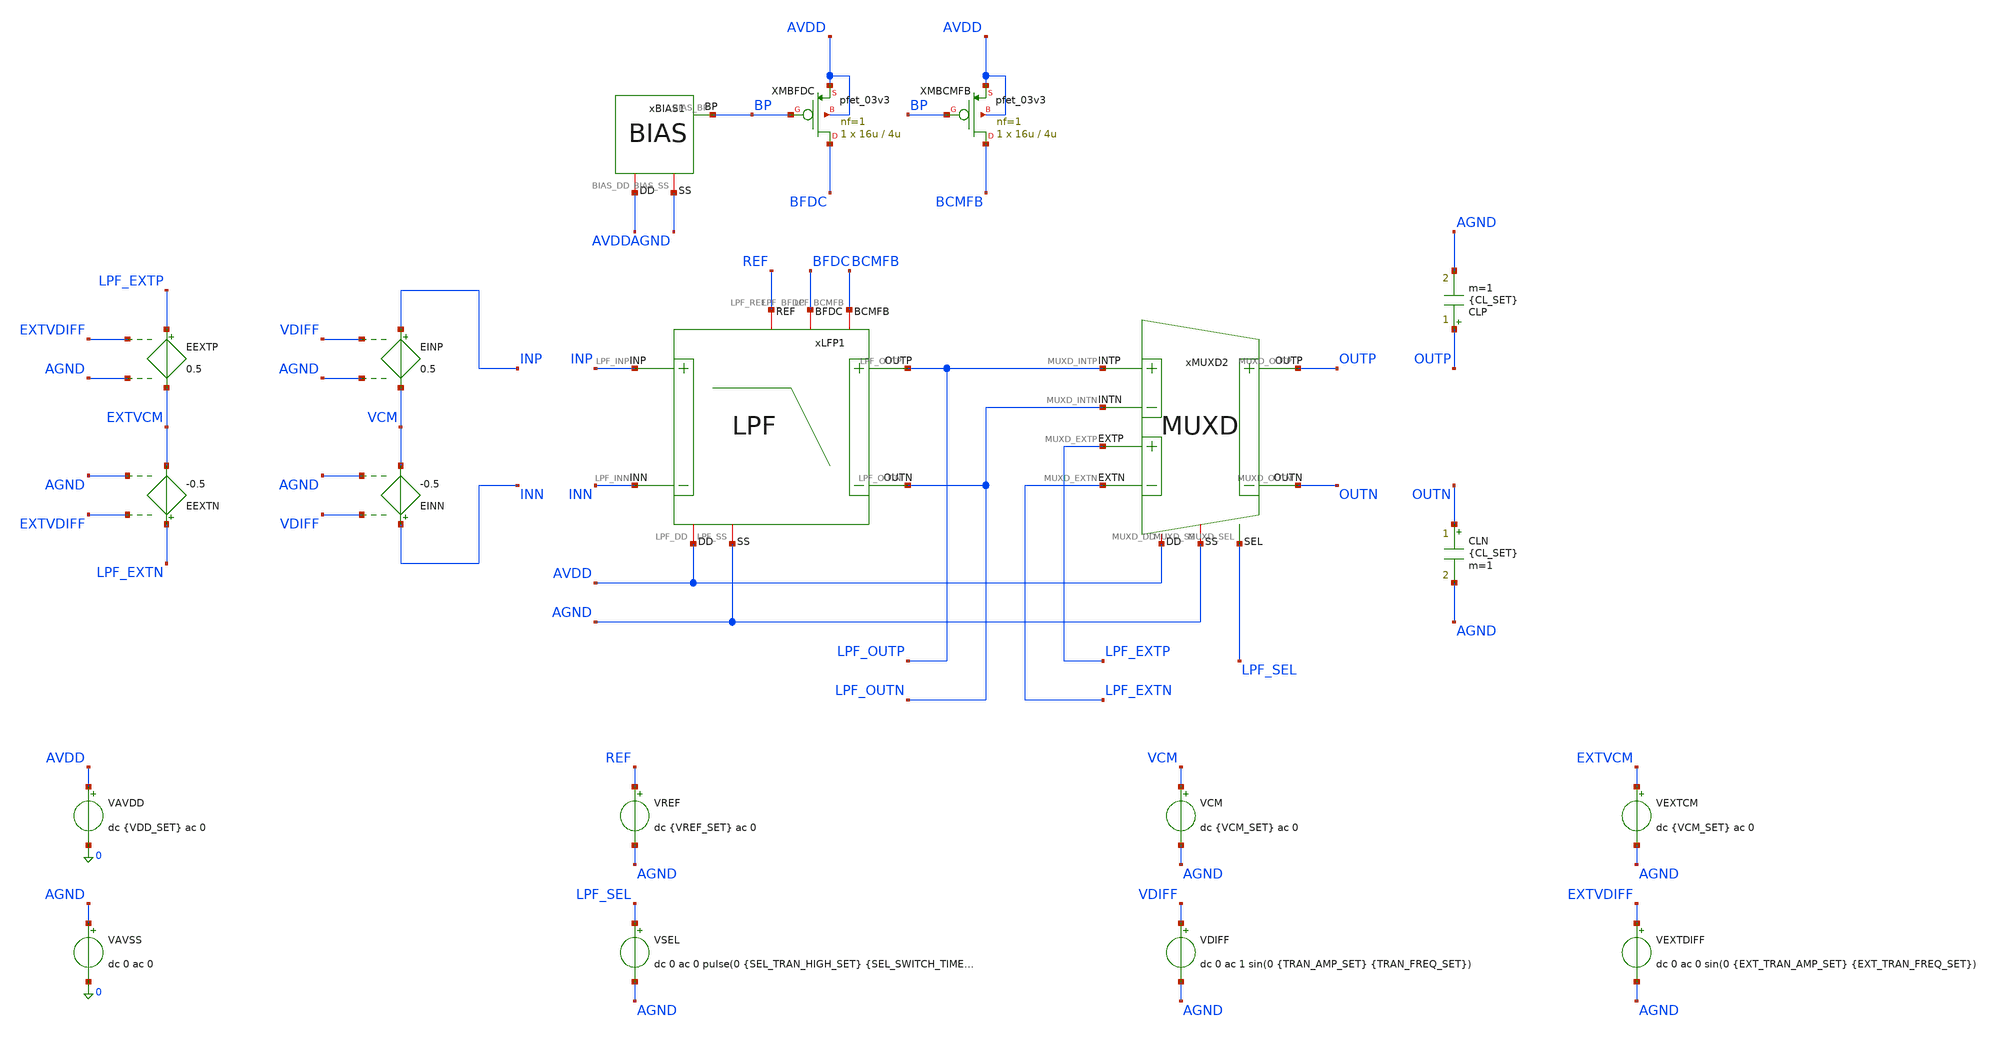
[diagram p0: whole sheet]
** sch_path: Design_Files/IC Design/Testbench/AFE_BLOCKS/LPF/LPF_TB_MC.sch
**.subckt LPF_TB_MC
CLP OUTP AGND {CL_SET} m=1
CLN OUTN AGND {CL_SET} m=1
xBIAS1 AVDD AGND BP BIAS
XMBFDC BFDC BP AVDD AVDD pfet_03v3 L=4u W=16u nf=1 ad='int((nf+1)/2) * W/nf * 0.18u' as='int((nf+2)/2) * W/nf * 0.18u'
+ pd='2*int((nf+1)/2) * (W/nf + 0.18u)' ps='2*int((nf+2)/2) * (W/nf + 0.18u)' nrd='0.18u / W' nrs='0.18u / W'
+ sa=0 sb=0 sd=0 m=1
XMBCMFB BCMFB BP AVDD AVDD pfet_03v3 L=4u W=16u nf=1 ad='int((nf+1)/2) * W/nf * 0.18u' as='int((nf+2)/2) * W/nf * 0.18u'
+ pd='2*int((nf+1)/2) * (W/nf + 0.18u)' ps='2*int((nf+2)/2) * (W/nf + 0.18u)' nrd='0.18u / W' nrs='0.18u / W'
+ sa=0 sb=0 sd=0 m=1
VAVDD AVDD 0 dc {VDD_SET} ac 0
.save i(vavdd)
VAVSS AGND 0 dc 0 ac 0
xLFP1 AVDD AGND INP INN LPF_OUTN BFDC LPF_OUTP BCMFB REF LPF
xMUXD2 AVDD AGND LPF_OUTP LPF_OUTN OUTN OUTP LPF_EXTP LPF_EXTN LPF_SEL MUXD
VCM VCM AGND dc {VCM_SET} ac 0
VDIFF VDIFF AGND dc 0 ac 1 sin(0 {TRAN_AMP_SET} {TRAN_FREQ_SET})
VREF REF AGND dc {VREF_SET} ac 0
VSEL LPF_SEL AGND dc 0 ac 0 pulse(0 {SEL_TRAN_HIGH_SET} {SEL_SWITCH_TIME_SET} 1u 1u 400m 800m)
VEXTCM EXTVCM AGND dc {VCM_SET} ac 0
VEXTDIFF EXTVDIFF AGND dc 0 ac 0 sin(0 {EXT_TRAN_AMP_SET} {EXT_TRAN_FREQ_SET})
EINP INP VCM VDIFF AGND 0.5
EINN INN VCM VDIFF AGND -0.5
EEXTP LPF_EXTP EXTVCM EXTVDIFF AGND 0.5
EEXTN LPF_EXTN EXTVCM EXTVDIFF AGND -0.5
**** begin user architecture code

* {MODELS_START}
.include $::180MCU_MODELS/design.ngspice

.param sw_stat_global=0
.param sw_stat_mismatch=1

.param mc_skew=3
.param res_mc_skew=3
.param cap_mc_skew=3

.lib $::180MCU_MODELS/sm141064.ngspice statistical
.lib $::180MCU_MODELS/sm141064.ngspice res_statistical
.lib $::180MCU_MODELS/sm141064.ngspice mimcap_statistical
.lib $::180MCU_MODELS/sm141064.ngspice cap_mim
.lib $::180MCU_MODELS/sm141064.ngspice bjt_statistical
* {MODELS_END}



* {SETUP_START}
.param VDD_SET=3.3
.param TEMP_SET=27

.param VCM_SET={VDD_SET/2}
.param VREF_SET={VDD_SET/2}

.param CL_SET=10p

.param LPF_GAIN_TARGET_SET=1
.param LPF_F1DB_TARGET_SET=150
.param LPF_F3DB_TARGET_SET=300

.param TRAN_AMP_SET=100m
.param TRAN_FREQ_SET=10

.param EXT_TRAN_AMP_SET=50m
.param EXT_TRAN_FREQ_SET=25

.param SEL_TRAN_HIGH_SET=0
.param SEL_SWITCH_TIME_SET=200m

.csparam MC_RUNS=200

.temp {TEMP_SET}

.options gmin=1e-12
.options rshunt=1e12
.options method=gear
* {SETUP_END}




* {MEAS_START}
.control

destroy all

set noaskquit
set wr_singlescale
unset wr_vecnames

option klu
option numdgt=15
option method=gear
option maxord=2
option plotwinsize=0

let mode_index=0

dowhile mode_index < 3

if mode_index = 0
set mode=mm
set tag=mm
alterparam sw_stat_global=0
alterparam sw_stat_mismatch=1
end

if mode_index = 1
set mode=gl
set tag=gl
alterparam sw_stat_global=1
alterparam sw_stat_mismatch=0
end

if mode_index = 2
set mode=full
set tag=full
alterparam sw_stat_global=1
alterparam sw_stat_mismatch=1
end

alterparam VDD_SET=3.3
alterparam TEMP_SET=27
alterparam SEL_TRAN_HIGH_SET=0
alterparam EXT_TRAN_AMP_SET=0

reset

shell mkdir -p /foss/designs/ECG_Acquisition_IC/Measurement_Results/IC_Simulation/AFE_BLOCKS/LPF/{$mode}.Result_txt
shell rm -f /foss/designs/ECG_Acquisition_IC/Measurement_Results/IC_Simulation/AFE_BLOCKS/LPF/{$mode}.Result_txt/{$tag}.mc_summary.txt

let run=1

dowhile run <= $&MC_RUNS

setseed $&run
mc_source

alter @VAVDD[DC]=3.3
alter @VAVSS[DC]=0

alter @VCM[DC]=1.65
alter @VREF[DC]=1.65
alter @VDIFF[DC]=0
alter @VSEL[DC]=0

alter @VAVDD[ACMAG]=0
alter @VAVSS[ACMAG]=0
alter @VCM[ACMAG]=0
alter @VREF[ACMAG]=0
alter @VDIFF[ACMAG]=0
alter @VEXTDIFF[ACMAG]=0

save all
save @m.xmbfdc.m0[id]
save @m.xmbcmfb.m0[id]


* OFFSET

dc VDIFF -10m 10m 10u

let lpf_diff=v(LPF_OUTP)-v(LPF_OUTN)

meas dc vos_meas when lpf_diff=0 cross=1

set vos_val=$&vos_meas

destroy all

alter @VDIFF[DC]=$vos_val


* OP

op

let out_cm=0.5*(v(LPF_OUTP)+v(LPF_OUTN))-v(AGND)
let out_cm_error=out_cm-v(REF)

let idd_total=abs(vavdd#branch)
let power_total=(v(AVDD)-v(AGND))*idd_total

let ibfdc=abs(@m.xmbfdc.m0[id])
let ibcmfb=abs(@m.xmbcmfb.m0[id])

set idd_val=$&idd_total
set power_val=$&power_total
set outcmerr_val=$&out_cm_error
set ibfdc_val=$&ibfdc
set ibcmfb_val=$&ibcmfb

destroy all


* DIFF AC

alter @VDIFF[ACMAG]=1
alter @VCM[ACMAG]=0
alter @VREF[ACMAG]=0
alter @VEXTDIFF[ACMAG]=0
alter @VAVDD[ACMAG]=0
alter @VAVSS[ACMAG]=0

ac dec 200 0.01 100k

let vin_diff=v(INP)-v(INN)
let lpf_diff=v(LPF_OUTP)-v(LPF_OUTN)

let lpf_gain=mag(lpf_diff/vin_diff)

meas ac gain10 find lpf_gain at=10
meas ac gain150 find lpf_gain at=150

let norm_db=20*log10(lpf_gain/$&gain10)

meas ac f1db when norm_db=-1 fall=1
meas ac f3db when norm_db=-3 fall=1

meas ac ad60 find lpf_gain at=60
meas ac ad150 find lpf_gain at=150

let gain_error_pct=100*($&gain10-1)
let gain150_rel_db=20*log10($&gain150/$&gain10)

set gain10_val=$&gain10
set gain150_val=$&gain150
set gainerr_val=$&gain_error_pct
set gain150db_val=$&gain150_rel_db

set f1db_val=$&f1db
set f3db_val=$&f3db

set ad60_val=$&ad60
set ad150_val=$&ad150

destroy all


* CMRR

alter @VDIFF[ACMAG]=0
alter @VCM[ACMAG]=1
alter @VREF[ACMAG]=0
alter @VEXTDIFF[ACMAG]=0
alter @VAVDD[ACMAG]=0
alter @VAVSS[ACMAG]=0

ac dec 200 0.01 100k

let vin_cm=0.5*(v(INP)+v(INN))-v(AGND)
let lpf_diff=v(LPF_OUTP)-v(LPF_OUTN)

let acm=mag(lpf_diff/vin_cm)

meas ac acm60 find acm at=60
meas ac acm150 find acm at=150

let cmrr60=20*log10($ad60_val/$&acm60)
let cmrr150=20*log10($ad150_val/$&acm150)

set cmrr60_val=$&cmrr60
set cmrr150_val=$&cmrr150

destroy all


* SUMMARY

echo $&run $ibfdc_val $ibcmfb_val $idd_val $power_val $outcmerr_val $vos_val $gain10_val $gainerr_val
+ $gain150_val $gain150db_val $f1db_val $f3db_val $cmrr60_val $cmrr150_val >> /foss/designs/ECG_Acquisition_IC/Measurement_Results/IC_Simulation/AFE_BLOCKS/LPF/{$mode}.Result_txt/{$tag}.mc_summary.txt

let run=run+1

end

let mode_index=mode_index+1

end

quit

.endc
* {MEAS_END}


**** end user architecture code
**.ends
.end
